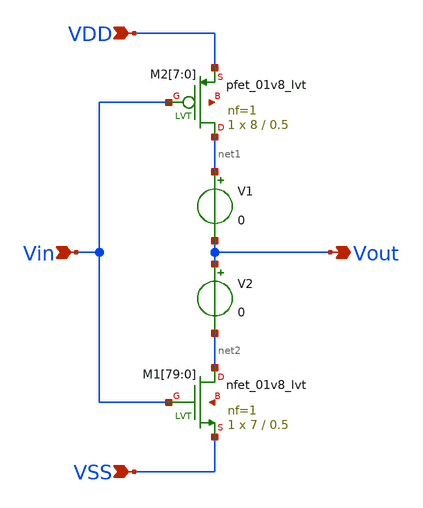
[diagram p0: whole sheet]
** sch_path: design/THESIS_EXP_RO_INVERTER_SKY130A/INV_LVT_v2.sch
**.subckt INV_LVT_v2 VDD VSS Vin Vout
*.ipin VDD
*.ipin VSS
*.ipin Vin
*.opin Vout
XM1[79] net2 Vin VSS net3[79] sky130_fd_pr__nfet_01v8_lvt L=0.5 W=7 nf=1 ad='int((nf+1)/2) * W/nf * 0.29'
+ as='int((nf+2)/2) * W/nf * 0.29' pd='2*int((nf+1)/2) * (W/nf + 0.29)' ps='2*int((nf+2)/2) * (W/nf + 0.29)'
+ nrd='0.29 / W' nrs='0.29 / W' sa=0 sb=0 sd=0 mult=1 m=1
XM1[78] net2 Vin VSS net3[78] sky130_fd_pr__nfet_01v8_lvt L=0.5 W=7 nf=1 ad='int((nf+1)/2) * W/nf * 0.29'
+ as='int((nf+2)/2) * W/nf * 0.29' pd='2*int((nf+1)/2) * (W/nf + 0.29)' ps='2*int((nf+2)/2) * (W/nf + 0.29)'
+ nrd='0.29 / W' nrs='0.29 / W' sa=0 sb=0 sd=0 mult=1 m=1
XM1[77] net2 Vin VSS net3[77] sky130_fd_pr__nfet_01v8_lvt L=0.5 W=7 nf=1 ad='int((nf+1)/2) * W/nf * 0.29'
+ as='int((nf+2)/2) * W/nf * 0.29' pd='2*int((nf+1)/2) * (W/nf + 0.29)' ps='2*int((nf+2)/2) * (W/nf + 0.29)'
+ nrd='0.29 / W' nrs='0.29 / W' sa=0 sb=0 sd=0 mult=1 m=1
XM1[76] net2 Vin VSS net3[76] sky130_fd_pr__nfet_01v8_lvt L=0.5 W=7 nf=1 ad='int((nf+1)/2) * W/nf * 0.29'
+ as='int((nf+2)/2) * W/nf * 0.29' pd='2*int((nf+1)/2) * (W/nf + 0.29)' ps='2*int((nf+2)/2) * (W/nf + 0.29)'
+ nrd='0.29 / W' nrs='0.29 / W' sa=0 sb=0 sd=0 mult=1 m=1
XM1[75] net2 Vin VSS net3[75] sky130_fd_pr__nfet_01v8_lvt L=0.5 W=7 nf=1 ad='int((nf+1)/2) * W/nf * 0.29'
+ as='int((nf+2)/2) * W/nf * 0.29' pd='2*int((nf+1)/2) * (W/nf + 0.29)' ps='2*int((nf+2)/2) * (W/nf + 0.29)'
+ nrd='0.29 / W' nrs='0.29 / W' sa=0 sb=0 sd=0 mult=1 m=1
XM1[74] net2 Vin VSS net3[74] sky130_fd_pr__nfet_01v8_lvt L=0.5 W=7 nf=1 ad='int((nf+1)/2) * W/nf * 0.29'
+ as='int((nf+2)/2) * W/nf * 0.29' pd='2*int((nf+1)/2) * (W/nf + 0.29)' ps='2*int((nf+2)/2) * (W/nf + 0.29)'
+ nrd='0.29 / W' nrs='0.29 / W' sa=0 sb=0 sd=0 mult=1 m=1
XM1[73] net2 Vin VSS net3[73] sky130_fd_pr__nfet_01v8_lvt L=0.5 W=7 nf=1 ad='int((nf+1)/2) * W/nf * 0.29'
+ as='int((nf+2)/2) * W/nf * 0.29' pd='2*int((nf+1)/2) * (W/nf + 0.29)' ps='2*int((nf+2)/2) * (W/nf + 0.29)'
+ nrd='0.29 / W' nrs='0.29 / W' sa=0 sb=0 sd=0 mult=1 m=1
XM1[72] net2 Vin VSS net3[72] sky130_fd_pr__nfet_01v8_lvt L=0.5 W=7 nf=1 ad='int((nf+1)/2) * W/nf * 0.29'
+ as='int((nf+2)/2) * W/nf * 0.29' pd='2*int((nf+1)/2) * (W/nf + 0.29)' ps='2*int((nf+2)/2) * (W/nf + 0.29)'
+ nrd='0.29 / W' nrs='0.29 / W' sa=0 sb=0 sd=0 mult=1 m=1
XM1[71] net2 Vin VSS net3[71] sky130_fd_pr__nfet_01v8_lvt L=0.5 W=7 nf=1 ad='int((nf+1)/2) * W/nf * 0.29'
+ as='int((nf+2)/2) * W/nf * 0.29' pd='2*int((nf+1)/2) * (W/nf + 0.29)' ps='2*int((nf+2)/2) * (W/nf + 0.29)'
+ nrd='0.29 / W' nrs='0.29 / W' sa=0 sb=0 sd=0 mult=1 m=1
XM1[70] net2 Vin VSS net3[70] sky130_fd_pr__nfet_01v8_lvt L=0.5 W=7 nf=1 ad='int((nf+1)/2) * W/nf * 0.29'
+ as='int((nf+2)/2) * W/nf * 0.29' pd='2*int((nf+1)/2) * (W/nf + 0.29)' ps='2*int((nf+2)/2) * (W/nf + 0.29)'
+ nrd='0.29 / W' nrs='0.29 / W' sa=0 sb=0 sd=0 mult=1 m=1
XM1[69] net2 Vin VSS net3[69] sky130_fd_pr__nfet_01v8_lvt L=0.5 W=7 nf=1 ad='int((nf+1)/2) * W/nf * 0.29'
+ as='int((nf+2)/2) * W/nf * 0.29' pd='2*int((nf+1)/2) * (W/nf + 0.29)' ps='2*int((nf+2)/2) * (W/nf + 0.29)'
+ nrd='0.29 / W' nrs='0.29 / W' sa=0 sb=0 sd=0 mult=1 m=1
XM1[68] net2 Vin VSS net3[68] sky130_fd_pr__nfet_01v8_lvt L=0.5 W=7 nf=1 ad='int((nf+1)/2) * W/nf * 0.29'
+ as='int((nf+2)/2) * W/nf * 0.29' pd='2*int((nf+1)/2) * (W/nf + 0.29)' ps='2*int((nf+2)/2) * (W/nf + 0.29)'
+ nrd='0.29 / W' nrs='0.29 / W' sa=0 sb=0 sd=0 mult=1 m=1
XM1[67] net2 Vin VSS net3[67] sky130_fd_pr__nfet_01v8_lvt L=0.5 W=7 nf=1 ad='int((nf+1)/2) * W/nf * 0.29'
+ as='int((nf+2)/2) * W/nf * 0.29' pd='2*int((nf+1)/2) * (W/nf + 0.29)' ps='2*int((nf+2)/2) * (W/nf + 0.29)'
+ nrd='0.29 / W' nrs='0.29 / W' sa=0 sb=0 sd=0 mult=1 m=1
XM1[66] net2 Vin VSS net3[66] sky130_fd_pr__nfet_01v8_lvt L=0.5 W=7 nf=1 ad='int((nf+1)/2) * W/nf * 0.29'
+ as='int((nf+2)/2) * W/nf * 0.29' pd='2*int((nf+1)/2) * (W/nf + 0.29)' ps='2*int((nf+2)/2) * (W/nf + 0.29)'
+ nrd='0.29 / W' nrs='0.29 / W' sa=0 sb=0 sd=0 mult=1 m=1
XM1[65] net2 Vin VSS net3[65] sky130_fd_pr__nfet_01v8_lvt L=0.5 W=7 nf=1 ad='int((nf+1)/2) * W/nf * 0.29'
+ as='int((nf+2)/2) * W/nf * 0.29' pd='2*int((nf+1)/2) * (W/nf + 0.29)' ps='2*int((nf+2)/2) * (W/nf + 0.29)'
+ nrd='0.29 / W' nrs='0.29 / W' sa=0 sb=0 sd=0 mult=1 m=1
XM1[64] net2 Vin VSS net3[64] sky130_fd_pr__nfet_01v8_lvt L=0.5 W=7 nf=1 ad='int((nf+1)/2) * W/nf * 0.29'
+ as='int((nf+2)/2) * W/nf * 0.29' pd='2*int((nf+1)/2) * (W/nf + 0.29)' ps='2*int((nf+2)/2) * (W/nf + 0.29)'
+ nrd='0.29 / W' nrs='0.29 / W' sa=0 sb=0 sd=0 mult=1 m=1
XM1[63] net2 Vin VSS net3[63] sky130_fd_pr__nfet_01v8_lvt L=0.5 W=7 nf=1 ad='int((nf+1)/2) * W/nf * 0.29'
+ as='int((nf+2)/2) * W/nf * 0.29' pd='2*int((nf+1)/2) * (W/nf + 0.29)' ps='2*int((nf+2)/2) * (W/nf + 0.29)'
+ nrd='0.29 / W' nrs='0.29 / W' sa=0 sb=0 sd=0 mult=1 m=1
XM1[62] net2 Vin VSS net3[62] sky130_fd_pr__nfet_01v8_lvt L=0.5 W=7 nf=1 ad='int((nf+1)/2) * W/nf * 0.29'
+ as='int((nf+2)/2) * W/nf * 0.29' pd='2*int((nf+1)/2) * (W/nf + 0.29)' ps='2*int((nf+2)/2) * (W/nf + 0.29)'
+ nrd='0.29 / W' nrs='0.29 / W' sa=0 sb=0 sd=0 mult=1 m=1
XM1[61] net2 Vin VSS net3[61] sky130_fd_pr__nfet_01v8_lvt L=0.5 W=7 nf=1 ad='int((nf+1)/2) * W/nf * 0.29'
+ as='int((nf+2)/2) * W/nf * 0.29' pd='2*int((nf+1)/2) * (W/nf + 0.29)' ps='2*int((nf+2)/2) * (W/nf + 0.29)'
+ nrd='0.29 / W' nrs='0.29 / W' sa=0 sb=0 sd=0 mult=1 m=1
XM1[60] net2 Vin VSS net3[60] sky130_fd_pr__nfet_01v8_lvt L=0.5 W=7 nf=1 ad='int((nf+1)/2) * W/nf * 0.29'
+ as='int((nf+2)/2) * W/nf * 0.29' pd='2*int((nf+1)/2) * (W/nf + 0.29)' ps='2*int((nf+2)/2) * (W/nf + 0.29)'
+ nrd='0.29 / W' nrs='0.29 / W' sa=0 sb=0 sd=0 mult=1 m=1
XM1[59] net2 Vin VSS net3[59] sky130_fd_pr__nfet_01v8_lvt L=0.5 W=7 nf=1 ad='int((nf+1)/2) * W/nf * 0.29'
+ as='int((nf+2)/2) * W/nf * 0.29' pd='2*int((nf+1)/2) * (W/nf + 0.29)' ps='2*int((nf+2)/2) * (W/nf + 0.29)'
+ nrd='0.29 / W' nrs='0.29 / W' sa=0 sb=0 sd=0 mult=1 m=1
XM1[58] net2 Vin VSS net3[58] sky130_fd_pr__nfet_01v8_lvt L=0.5 W=7 nf=1 ad='int((nf+1)/2) * W/nf * 0.29'
+ as='int((nf+2)/2) * W/nf * 0.29' pd='2*int((nf+1)/2) * (W/nf + 0.29)' ps='2*int((nf+2)/2) * (W/nf + 0.29)'
+ nrd='0.29 / W' nrs='0.29 / W' sa=0 sb=0 sd=0 mult=1 m=1
XM1[57] net2 Vin VSS net3[57] sky130_fd_pr__nfet_01v8_lvt L=0.5 W=7 nf=1 ad='int((nf+1)/2) * W/nf * 0.29'
+ as='int((nf+2)/2) * W/nf * 0.29' pd='2*int((nf+1)/2) * (W/nf + 0.29)' ps='2*int((nf+2)/2) * (W/nf + 0.29)'
+ nrd='0.29 / W' nrs='0.29 / W' sa=0 sb=0 sd=0 mult=1 m=1
XM1[56] net2 Vin VSS net3[56] sky130_fd_pr__nfet_01v8_lvt L=0.5 W=7 nf=1 ad='int((nf+1)/2) * W/nf * 0.29'
+ as='int((nf+2)/2) * W/nf * 0.29' pd='2*int((nf+1)/2) * (W/nf + 0.29)' ps='2*int((nf+2)/2) * (W/nf + 0.29)'
+ nrd='0.29 / W' nrs='0.29 / W' sa=0 sb=0 sd=0 mult=1 m=1
XM1[55] net2 Vin VSS net3[55] sky130_fd_pr__nfet_01v8_lvt L=0.5 W=7 nf=1 ad='int((nf+1)/2) * W/nf * 0.29'
+ as='int((nf+2)/2) * W/nf * 0.29' pd='2*int((nf+1)/2) * (W/nf + 0.29)' ps='2*int((nf+2)/2) * (W/nf + 0.29)'
+ nrd='0.29 / W' nrs='0.29 / W' sa=0 sb=0 sd=0 mult=1 m=1
XM1[54] net2 Vin VSS net3[54] sky130_fd_pr__nfet_01v8_lvt L=0.5 W=7 nf=1 ad='int((nf+1)/2) * W/nf * 0.29'
+ as='int((nf+2)/2) * W/nf * 0.29' pd='2*int((nf+1)/2) * (W/nf + 0.29)' ps='2*int((nf+2)/2) * (W/nf + 0.29)'
+ nrd='0.29 / W' nrs='0.29 / W' sa=0 sb=0 sd=0 mult=1 m=1
XM1[53] net2 Vin VSS net3[53] sky130_fd_pr__nfet_01v8_lvt L=0.5 W=7 nf=1 ad='int((nf+1)/2) * W/nf * 0.29'
+ as='int((nf+2)/2) * W/nf * 0.29' pd='2*int((nf+1)/2) * (W/nf + 0.29)' ps='2*int((nf+2)/2) * (W/nf + 0.29)'
+ nrd='0.29 / W' nrs='0.29 / W' sa=0 sb=0 sd=0 mult=1 m=1
XM1[52] net2 Vin VSS net3[52] sky130_fd_pr__nfet_01v8_lvt L=0.5 W=7 nf=1 ad='int((nf+1)/2) * W/nf * 0.29'
+ as='int((nf+2)/2) * W/nf * 0.29' pd='2*int((nf+1)/2) * (W/nf + 0.29)' ps='2*int((nf+2)/2) * (W/nf + 0.29)'
+ nrd='0.29 / W' nrs='0.29 / W' sa=0 sb=0 sd=0 mult=1 m=1
XM1[51] net2 Vin VSS net3[51] sky130_fd_pr__nfet_01v8_lvt L=0.5 W=7 nf=1 ad='int((nf+1)/2) * W/nf * 0.29'
+ as='int((nf+2)/2) * W/nf * 0.29' pd='2*int((nf+1)/2) * (W/nf + 0.29)' ps='2*int((nf+2)/2) * (W/nf + 0.29)'
+ nrd='0.29 / W' nrs='0.29 / W' sa=0 sb=0 sd=0 mult=1 m=1
XM1[50] net2 Vin VSS net3[50] sky130_fd_pr__nfet_01v8_lvt L=0.5 W=7 nf=1 ad='int((nf+1)/2) * W/nf * 0.29'
+ as='int((nf+2)/2) * W/nf * 0.29' pd='2*int((nf+1)/2) * (W/nf + 0.29)' ps='2*int((nf+2)/2) * (W/nf + 0.29)'
+ nrd='0.29 / W' nrs='0.29 / W' sa=0 sb=0 sd=0 mult=1 m=1
XM1[49] net2 Vin VSS net3[49] sky130_fd_pr__nfet_01v8_lvt L=0.5 W=7 nf=1 ad='int((nf+1)/2) * W/nf * 0.29'
+ as='int((nf+2)/2) * W/nf * 0.29' pd='2*int((nf+1)/2) * (W/nf + 0.29)' ps='2*int((nf+2)/2) * (W/nf + 0.29)'
+ nrd='0.29 / W' nrs='0.29 / W' sa=0 sb=0 sd=0 mult=1 m=1
XM1[48] net2 Vin VSS net3[48] sky130_fd_pr__nfet_01v8_lvt L=0.5 W=7 nf=1 ad='int((nf+1)/2) * W/nf * 0.29'
+ as='int((nf+2)/2) * W/nf * 0.29' pd='2*int((nf+1)/2) * (W/nf + 0.29)' ps='2*int((nf+2)/2) * (W/nf + 0.29)'
+ nrd='0.29 / W' nrs='0.29 / W' sa=0 sb=0 sd=0 mult=1 m=1
XM1[47] net2 Vin VSS net3[47] sky130_fd_pr__nfet_01v8_lvt L=0.5 W=7 nf=1 ad='int((nf+1)/2) * W/nf * 0.29'
+ as='int((nf+2)/2) * W/nf * 0.29' pd='2*int((nf+1)/2) * (W/nf + 0.29)' ps='2*int((nf+2)/2) * (W/nf + 0.29)'
+ nrd='0.29 / W' nrs='0.29 / W' sa=0 sb=0 sd=0 mult=1 m=1
XM1[46] net2 Vin VSS net3[46] sky130_fd_pr__nfet_01v8_lvt L=0.5 W=7 nf=1 ad='int((nf+1)/2) * W/nf * 0.29'
+ as='int((nf+2)/2) * W/nf * 0.29' pd='2*int((nf+1)/2) * (W/nf + 0.29)' ps='2*int((nf+2)/2) * (W/nf + 0.29)'
+ nrd='0.29 / W' nrs='0.29 / W' sa=0 sb=0 sd=0 mult=1 m=1
XM1[45] net2 Vin VSS net3[45] sky130_fd_pr__nfet_01v8_lvt L=0.5 W=7 nf=1 ad='int((nf+1)/2) * W/nf * 0.29'
+ as='int((nf+2)/2) * W/nf * 0.29' pd='2*int((nf+1)/2) * (W/nf + 0.29)' ps='2*int((nf+2)/2) * (W/nf + 0.29)'
+ nrd='0.29 / W' nrs='0.29 / W' sa=0 sb=0 sd=0 mult=1 m=1
XM1[44] net2 Vin VSS net3[44] sky130_fd_pr__nfet_01v8_lvt L=0.5 W=7 nf=1 ad='int((nf+1)/2) * W/nf * 0.29'
+ as='int((nf+2)/2) * W/nf * 0.29' pd='2*int((nf+1)/2) * (W/nf + 0.29)' ps='2*int((nf+2)/2) * (W/nf + 0.29)'
+ nrd='0.29 / W' nrs='0.29 / W' sa=0 sb=0 sd=0 mult=1 m=1
XM1[43] net2 Vin VSS net3[43] sky130_fd_pr__nfet_01v8_lvt L=0.5 W=7 nf=1 ad='int((nf+1)/2) * W/nf * 0.29'
+ as='int((nf+2)/2) * W/nf * 0.29' pd='2*int((nf+1)/2) * (W/nf + 0.29)' ps='2*int((nf+2)/2) * (W/nf + 0.29)'
+ nrd='0.29 / W' nrs='0.29 / W' sa=0 sb=0 sd=0 mult=1 m=1
XM1[42] net2 Vin VSS net3[42] sky130_fd_pr__nfet_01v8_lvt L=0.5 W=7 nf=1 ad='int((nf+1)/2) * W/nf * 0.29'
+ as='int((nf+2)/2) * W/nf * 0.29' pd='2*int((nf+1)/2) * (W/nf + 0.29)' ps='2*int((nf+2)/2) * (W/nf + 0.29)'
+ nrd='0.29 / W' nrs='0.29 / W' sa=0 sb=0 sd=0 mult=1 m=1
XM1[41] net2 Vin VSS net3[41] sky130_fd_pr__nfet_01v8_lvt L=0.5 W=7 nf=1 ad='int((nf+1)/2) * W/nf * 0.29'
+ as='int((nf+2)/2) * W/nf * 0.29' pd='2*int((nf+1)/2) * (W/nf + 0.29)' ps='2*int((nf+2)/2) * (W/nf + 0.29)'
+ nrd='0.29 / W' nrs='0.29 / W' sa=0 sb=0 sd=0 mult=1 m=1
XM1[40] net2 Vin VSS net3[40] sky130_fd_pr__nfet_01v8_lvt L=0.5 W=7 nf=1 ad='int((nf+1)/2) * W/nf * 0.29'
+ as='int((nf+2)/2) * W/nf * 0.29' pd='2*int((nf+1)/2) * (W/nf + 0.29)' ps='2*int((nf+2)/2) * (W/nf + 0.29)'
+ nrd='0.29 / W' nrs='0.29 / W' sa=0 sb=0 sd=0 mult=1 m=1
XM1[39] net2 Vin VSS net3[39] sky130_fd_pr__nfet_01v8_lvt L=0.5 W=7 nf=1 ad='int((nf+1)/2) * W/nf * 0.29'
+ as='int((nf+2)/2) * W/nf * 0.29' pd='2*int((nf+1)/2) * (W/nf + 0.29)' ps='2*int((nf+2)/2) * (W/nf + 0.29)'
+ nrd='0.29 / W' nrs='0.29 / W' sa=0 sb=0 sd=0 mult=1 m=1
XM1[38] net2 Vin VSS net3[38] sky130_fd_pr__nfet_01v8_lvt L=0.5 W=7 nf=1 ad='int((nf+1)/2) * W/nf * 0.29'
+ as='int((nf+2)/2) * W/nf * 0.29' pd='2*int((nf+1)/2) * (W/nf + 0.29)' ps='2*int((nf+2)/2) * (W/nf + 0.29)'
+ nrd='0.29 / W' nrs='0.29 / W' sa=0 sb=0 sd=0 mult=1 m=1
XM1[37] net2 Vin VSS net3[37] sky130_fd_pr__nfet_01v8_lvt L=0.5 W=7 nf=1 ad='int((nf+1)/2) * W/nf * 0.29'
+ as='int((nf+2)/2) * W/nf * 0.29' pd='2*int((nf+1)/2) * (W/nf + 0.29)' ps='2*int((nf+2)/2) * (W/nf + 0.29)'
+ nrd='0.29 / W' nrs='0.29 / W' sa=0 sb=0 sd=0 mult=1 m=1
XM1[36] net2 Vin VSS net3[36] sky130_fd_pr__nfet_01v8_lvt L=0.5 W=7 nf=1 ad='int((nf+1)/2) * W/nf * 0.29'
+ as='int((nf+2)/2) * W/nf * 0.29' pd='2*int((nf+1)/2) * (W/nf + 0.29)' ps='2*int((nf+2)/2) * (W/nf + 0.29)'
+ nrd='0.29 / W' nrs='0.29 / W' sa=0 sb=0 sd=0 mult=1 m=1
XM1[35] net2 Vin VSS net3[35] sky130_fd_pr__nfet_01v8_lvt L=0.5 W=7 nf=1 ad='int((nf+1)/2) * W/nf * 0.29'
+ as='int((nf+2)/2) * W/nf * 0.29' pd='2*int((nf+1)/2) * (W/nf + 0.29)' ps='2*int((nf+2)/2) * (W/nf + 0.29)'
+ nrd='0.29 / W' nrs='0.29 / W' sa=0 sb=0 sd=0 mult=1 m=1
XM1[34] net2 Vin VSS net3[34] sky130_fd_pr__nfet_01v8_lvt L=0.5 W=7 nf=1 ad='int((nf+1)/2) * W/nf * 0.29'
+ as='int((nf+2)/2) * W/nf * 0.29' pd='2*int((nf+1)/2) * (W/nf + 0.29)' ps='2*int((nf+2)/2) * (W/nf + 0.29)'
+ nrd='0.29 / W' nrs='0.29 / W' sa=0 sb=0 sd=0 mult=1 m=1
XM1[33] net2 Vin VSS net3[33] sky130_fd_pr__nfet_01v8_lvt L=0.5 W=7 nf=1 ad='int((nf+1)/2) * W/nf * 0.29'
+ as='int((nf+2)/2) * W/nf * 0.29' pd='2*int((nf+1)/2) * (W/nf + 0.29)' ps='2*int((nf+2)/2) * (W/nf + 0.29)'
+ nrd='0.29 / W' nrs='0.29 / W' sa=0 sb=0 sd=0 mult=1 m=1
XM1[32] net2 Vin VSS net3[32] sky130_fd_pr__nfet_01v8_lvt L=0.5 W=7 nf=1 ad='int((nf+1)/2) * W/nf * 0.29'
+ as='int((nf+2)/2) * W/nf * 0.29' pd='2*int((nf+1)/2) * (W/nf + 0.29)' ps='2*int((nf+2)/2) * (W/nf + 0.29)'
+ nrd='0.29 / W' nrs='0.29 / W' sa=0 sb=0 sd=0 mult=1 m=1
XM1[31] net2 Vin VSS net3[31] sky130_fd_pr__nfet_01v8_lvt L=0.5 W=7 nf=1 ad='int((nf+1)/2) * W/nf * 0.29'
+ as='int((nf+2)/2) * W/nf * 0.29' pd='2*int((nf+1)/2) * (W/nf + 0.29)' ps='2*int((nf+2)/2) * (W/nf + 0.29)'
+ nrd='0.29 / W' nrs='0.29 / W' sa=0 sb=0 sd=0 mult=1 m=1
XM1[30] net2 Vin VSS net3[30] sky130_fd_pr__nfet_01v8_lvt L=0.5 W=7 nf=1 ad='int((nf+1)/2) * W/nf * 0.29'
+ as='int((nf+2)/2) * W/nf * 0.29' pd='2*int((nf+1)/2) * (W/nf + 0.29)' ps='2*int((nf+2)/2) * (W/nf + 0.29)'
+ nrd='0.29 / W' nrs='0.29 / W' sa=0 sb=0 sd=0 mult=1 m=1
XM1[29] net2 Vin VSS net3[29] sky130_fd_pr__nfet_01v8_lvt L=0.5 W=7 nf=1 ad='int((nf+1)/2) * W/nf * 0.29'
+ as='int((nf+2)/2) * W/nf * 0.29' pd='2*int((nf+1)/2) * (W/nf + 0.29)' ps='2*int((nf+2)/2) * (W/nf + 0.29)'
+ nrd='0.29 / W' nrs='0.29 / W' sa=0 sb=0 sd=0 mult=1 m=1
XM1[28] net2 Vin VSS net3[28] sky130_fd_pr__nfet_01v8_lvt L=0.5 W=7 nf=1 ad='int((nf+1)/2) * W/nf * 0.29'
+ as='int((nf+2)/2) * W/nf * 0.29' pd='2*int((nf+1)/2) * (W/nf + 0.29)' ps='2*int((nf+2)/2) * (W/nf + 0.29)'
+ nrd='0.29 / W' nrs='0.29 / W' sa=0 sb=0 sd=0 mult=1 m=1
XM1[27] net2 Vin VSS net3[27] sky130_fd_pr__nfet_01v8_lvt L=0.5 W=7 nf=1 ad='int((nf+1)/2) * W/nf * 0.29'
+ as='int((nf+2)/2) * W/nf * 0.29' pd='2*int((nf+1)/2) * (W/nf + 0.29)' ps='2*int((nf+2)/2) * (W/nf + 0.29)'
+ nrd='0.29 / W' nrs='0.29 / W' sa=0 sb=0 sd=0 mult=1 m=1
XM1[26] net2 Vin VSS net3[26] sky130_fd_pr__nfet_01v8_lvt L=0.5 W=7 nf=1 ad='int((nf+1)/2) * W/nf * 0.29'
+ as='int((nf+2)/2) * W/nf * 0.29' pd='2*int((nf+1)/2) * (W/nf + 0.29)' ps='2*int((nf+2)/2) * (W/nf + 0.29)'
+ nrd='0.29 / W' nrs='0.29 / W' sa=0 sb=0 sd=0 mult=1 m=1
XM1[25] net2 Vin VSS net3[25] sky130_fd_pr__nfet_01v8_lvt L=0.5 W=7 nf=1 ad='int((nf+1)/2) * W/nf * 0.29'
+ as='int((nf+2)/2) * W/nf * 0.29' pd='2*int((nf+1)/2) * (W/nf + 0.29)' ps='2*int((nf+2)/2) * (W/nf + 0.29)'
+ nrd='0.29 / W' nrs='0.29 / W' sa=0 sb=0 sd=0 mult=1 m=1
XM1[24] net2 Vin VSS net3[24] sky130_fd_pr__nfet_01v8_lvt L=0.5 W=7 nf=1 ad='int((nf+1)/2) * W/nf * 0.29'
+ as='int((nf+2)/2) * W/nf * 0.29' pd='2*int((nf+1)/2) * (W/nf + 0.29)' ps='2*int((nf+2)/2) * (W/nf + 0.29)'
+ nrd='0.29 / W' nrs='0.29 / W' sa=0 sb=0 sd=0 mult=1 m=1
XM1[23] net2 Vin VSS net3[23] sky130_fd_pr__nfet_01v8_lvt L=0.5 W=7 nf=1 ad='int((nf+1)/2) * W/nf * 0.29'
+ as='int((nf+2)/2) * W/nf * 0.29' pd='2*int((nf+1)/2) * (W/nf + 0.29)' ps='2*int((nf+2)/2) * (W/nf + 0.29)'
+ nrd='0.29 / W' nrs='0.29 / W' sa=0 sb=0 sd=0 mult=1 m=1
XM1[22] net2 Vin VSS net3[22] sky130_fd_pr__nfet_01v8_lvt L=0.5 W=7 nf=1 ad='int((nf+1)/2) * W/nf * 0.29'
+ as='int((nf+2)/2) * W/nf * 0.29' pd='2*int((nf+1)/2) * (W/nf + 0.29)' ps='2*int((nf+2)/2) * (W/nf + 0.29)'
+ nrd='0.29 / W' nrs='0.29 / W' sa=0 sb=0 sd=0 mult=1 m=1
XM1[21] net2 Vin VSS net3[21] sky130_fd_pr__nfet_01v8_lvt L=0.5 W=7 nf=1 ad='int((nf+1)/2) * W/nf * 0.29'
+ as='int((nf+2)/2) * W/nf * 0.29' pd='2*int((nf+1)/2) * (W/nf + 0.29)' ps='2*int((nf+2)/2) * (W/nf + 0.29)'
+ nrd='0.29 / W' nrs='0.29 / W' sa=0 sb=0 sd=0 mult=1 m=1
XM1[20] net2 Vin VSS net3[20] sky130_fd_pr__nfet_01v8_lvt L=0.5 W=7 nf=1 ad='int((nf+1)/2) * W/nf * 0.29'
+ as='int((nf+2)/2) * W/nf * 0.29' pd='2*int((nf+1)/2) * (W/nf + 0.29)' ps='2*int((nf+2)/2) * (W/nf + 0.29)'
+ nrd='0.29 / W' nrs='0.29 / W' sa=0 sb=0 sd=0 mult=1 m=1
XM1[19] net2 Vin VSS net3[19] sky130_fd_pr__nfet_01v8_lvt L=0.5 W=7 nf=1 ad='int((nf+1)/2) * W/nf * 0.29'
+ as='int((nf+2)/2) * W/nf * 0.29' pd='2*int((nf+1)/2) * (W/nf + 0.29)' ps='2*int((nf+2)/2) * (W/nf + 0.29)'
+ nrd='0.29 / W' nrs='0.29 / W' sa=0 sb=0 sd=0 mult=1 m=1
XM1[18] net2 Vin VSS net3[18] sky130_fd_pr__nfet_01v8_lvt L=0.5 W=7 nf=1 ad='int((nf+1)/2) * W/nf * 0.29'
+ as='int((nf+2)/2) * W/nf * 0.29' pd='2*int((nf+1)/2) * (W/nf + 0.29)' ps='2*int((nf+2)/2) * (W/nf + 0.29)'
+ nrd='0.29 / W' nrs='0.29 / W' sa=0 sb=0 sd=0 mult=1 m=1
XM1[17] net2 Vin VSS net3[17] sky130_fd_pr__nfet_01v8_lvt L=0.5 W=7 nf=1 ad='int((nf+1)/2) * W/nf * 0.29'
+ as='int((nf+2)/2) * W/nf * 0.29' pd='2*int((nf+1)/2) * (W/nf + 0.29)' ps='2*int((nf+2)/2) * (W/nf + 0.29)'
+ nrd='0.29 / W' nrs='0.29 / W' sa=0 sb=0 sd=0 mult=1 m=1
XM1[16] net2 Vin VSS net3[16] sky130_fd_pr__nfet_01v8_lvt L=0.5 W=7 nf=1 ad='int((nf+1)/2) * W/nf * 0.29'
+ as='int((nf+2)/2) * W/nf * 0.29' pd='2*int((nf+1)/2) * (W/nf + 0.29)' ps='2*int((nf+2)/2) * (W/nf + 0.29)'
+ nrd='0.29 / W' nrs='0.29 / W' sa=0 sb=0 sd=0 mult=1 m=1
XM1[15] net2 Vin VSS net3[15] sky130_fd_pr__nfet_01v8_lvt L=0.5 W=7 nf=1 ad='int((nf+1)/2) * W/nf * 0.29'
+ as='int((nf+2)/2) * W/nf * 0.29' pd='2*int((nf+1)/2) * (W/nf + 0.29)' ps='2*int((nf+2)/2) * (W/nf + 0.29)'
+ nrd='0.29 / W' nrs='0.29 / W' sa=0 sb=0 sd=0 mult=1 m=1
XM1[14] net2 Vin VSS net3[14] sky130_fd_pr__nfet_01v8_lvt L=0.5 W=7 nf=1 ad='int((nf+1)/2) * W/nf * 0.29'
+ as='int((nf+2)/2) * W/nf * 0.29' pd='2*int((nf+1)/2) * (W/nf + 0.29)' ps='2*int((nf+2)/2) * (W/nf + 0.29)'
+ nrd='0.29 / W' nrs='0.29 / W' sa=0 sb=0 sd=0 mult=1 m=1
XM1[13] net2 Vin VSS net3[13] sky130_fd_pr__nfet_01v8_lvt L=0.5 W=7 nf=1 ad='int((nf+1)/2) * W/nf * 0.29'
+ as='int((nf+2)/2) * W/nf * 0.29' pd='2*int((nf+1)/2) * (W/nf + 0.29)' ps='2*int((nf+2)/2) * (W/nf + 0.29)'
+ nrd='0.29 / W' nrs='0.29 / W' sa=0 sb=0 sd=0 mult=1 m=1
XM1[12] net2 Vin VSS net3[12] sky130_fd_pr__nfet_01v8_lvt L=0.5 W=7 nf=1 ad='int((nf+1)/2) * W/nf * 0.29'
+ as='int((nf+2)/2) * W/nf * 0.29' pd='2*int((nf+1)/2) * (W/nf + 0.29)' ps='2*int((nf+2)/2) * (W/nf + 0.29)'
+ nrd='0.29 / W' nrs='0.29 / W' sa=0 sb=0 sd=0 mult=1 m=1
XM1[11] net2 Vin VSS net3[11] sky130_fd_pr__nfet_01v8_lvt L=0.5 W=7 nf=1 ad='int((nf+1)/2) * W/nf * 0.29'
+ as='int((nf+2)/2) * W/nf * 0.29' pd='2*int((nf+1)/2) * (W/nf + 0.29)' ps='2*int((nf+2)/2) * (W/nf + 0.29)'
+ nrd='0.29 / W' nrs='0.29 / W' sa=0 sb=0 sd=0 mult=1 m=1
XM1[10] net2 Vin VSS net3[10] sky130_fd_pr__nfet_01v8_lvt L=0.5 W=7 nf=1 ad='int((nf+1)/2) * W/nf * 0.29'
+ as='int((nf+2)/2) * W/nf * 0.29' pd='2*int((nf+1)/2) * (W/nf + 0.29)' ps='2*int((nf+2)/2) * (W/nf + 0.29)'
+ nrd='0.29 / W' nrs='0.29 / W' sa=0 sb=0 sd=0 mult=1 m=1
XM1[9] net2 Vin VSS net3[9] sky130_fd_pr__nfet_01v8_lvt L=0.5 W=7 nf=1 ad='int((nf+1)/2) * W/nf * 0.29'
+ as='int((nf+2)/2) * W/nf * 0.29' pd='2*int((nf+1)/2) * (W/nf + 0.29)' ps='2*int((nf+2)/2) * (W/nf + 0.29)'
+ nrd='0.29 / W' nrs='0.29 / W' sa=0 sb=0 sd=0 mult=1 m=1
XM1[8] net2 Vin VSS net3[8] sky130_fd_pr__nfet_01v8_lvt L=0.5 W=7 nf=1 ad='int((nf+1)/2) * W/nf * 0.29'
+ as='int((nf+2)/2) * W/nf * 0.29' pd='2*int((nf+1)/2) * (W/nf + 0.29)' ps='2*int((nf+2)/2) * (W/nf + 0.29)'
+ nrd='0.29 / W' nrs='0.29 / W' sa=0 sb=0 sd=0 mult=1 m=1
XM1[7] net2 Vin VSS net3[7] sky130_fd_pr__nfet_01v8_lvt L=0.5 W=7 nf=1 ad='int((nf+1)/2) * W/nf * 0.29'
+ as='int((nf+2)/2) * W/nf * 0.29' pd='2*int((nf+1)/2) * (W/nf + 0.29)' ps='2*int((nf+2)/2) * (W/nf + 0.29)'
+ nrd='0.29 / W' nrs='0.29 / W' sa=0 sb=0 sd=0 mult=1 m=1
XM1[6] net2 Vin VSS net3[6] sky130_fd_pr__nfet_01v8_lvt L=0.5 W=7 nf=1 ad='int((nf+1)/2) * W/nf * 0.29'
+ as='int((nf+2)/2) * W/nf * 0.29' pd='2*int((nf+1)/2) * (W/nf + 0.29)' ps='2*int((nf+2)/2) * (W/nf + 0.29)'
+ nrd='0.29 / W' nrs='0.29 / W' sa=0 sb=0 sd=0 mult=1 m=1
XM1[5] net2 Vin VSS net3[5] sky130_fd_pr__nfet_01v8_lvt L=0.5 W=7 nf=1 ad='int((nf+1)/2) * W/nf * 0.29'
+ as='int((nf+2)/2) * W/nf * 0.29' pd='2*int((nf+1)/2) * (W/nf + 0.29)' ps='2*int((nf+2)/2) * (W/nf + 0.29)'
+ nrd='0.29 / W' nrs='0.29 / W' sa=0 sb=0 sd=0 mult=1 m=1
XM1[4] net2 Vin VSS net3[4] sky130_fd_pr__nfet_01v8_lvt L=0.5 W=7 nf=1 ad='int((nf+1)/2) * W/nf * 0.29'
+ as='int((nf+2)/2) * W/nf * 0.29' pd='2*int((nf+1)/2) * (W/nf + 0.29)' ps='2*int((nf+2)/2) * (W/nf + 0.29)'
+ nrd='0.29 / W' nrs='0.29 / W' sa=0 sb=0 sd=0 mult=1 m=1
XM1[3] net2 Vin VSS net3[3] sky130_fd_pr__nfet_01v8_lvt L=0.5 W=7 nf=1 ad='int((nf+1)/2) * W/nf * 0.29'
+ as='int((nf+2)/2) * W/nf * 0.29' pd='2*int((nf+1)/2) * (W/nf + 0.29)' ps='2*int((nf+2)/2) * (W/nf + 0.29)'
+ nrd='0.29 / W' nrs='0.29 / W' sa=0 sb=0 sd=0 mult=1 m=1
XM1[2] net2 Vin VSS net3[2] sky130_fd_pr__nfet_01v8_lvt L=0.5 W=7 nf=1 ad='int((nf+1)/2) * W/nf * 0.29'
+ as='int((nf+2)/2) * W/nf * 0.29' pd='2*int((nf+1)/2) * (W/nf + 0.29)' ps='2*int((nf+2)/2) * (W/nf + 0.29)'
+ nrd='0.29 / W' nrs='0.29 / W' sa=0 sb=0 sd=0 mult=1 m=1
XM1[1] net2 Vin VSS net3[1] sky130_fd_pr__nfet_01v8_lvt L=0.5 W=7 nf=1 ad='int((nf+1)/2) * W/nf * 0.29'
+ as='int((nf+2)/2) * W/nf * 0.29' pd='2*int((nf+1)/2) * (W/nf + 0.29)' ps='2*int((nf+2)/2) * (W/nf + 0.29)'
+ nrd='0.29 / W' nrs='0.29 / W' sa=0 sb=0 sd=0 mult=1 m=1
XM1[0] net2 Vin VSS net3[0] sky130_fd_pr__nfet_01v8_lvt L=0.5 W=7 nf=1 ad='int((nf+1)/2) * W/nf * 0.29'
+ as='int((nf+2)/2) * W/nf * 0.29' pd='2*int((nf+1)/2) * (W/nf + 0.29)' ps='2*int((nf+2)/2) * (W/nf + 0.29)'
+ nrd='0.29 / W' nrs='0.29 / W' sa=0 sb=0 sd=0 mult=1 m=1
XM2[7] net1 Vin VDD net4[7] sky130_fd_pr__pfet_01v8_lvt L=0.5 W=8 nf=1 ad='int((nf+1)/2) * W/nf * 0.29'
+ as='int((nf+2)/2) * W/nf * 0.29' pd='2*int((nf+1)/2) * (W/nf + 0.29)' ps='2*int((nf+2)/2) * (W/nf + 0.29)'
+ nrd='0.29 / W' nrs='0.29 / W' sa=0 sb=0 sd=0 mult=1 m=1
XM2[6] net1 Vin VDD net4[6] sky130_fd_pr__pfet_01v8_lvt L=0.5 W=8 nf=1 ad='int((nf+1)/2) * W/nf * 0.29'
+ as='int((nf+2)/2) * W/nf * 0.29' pd='2*int((nf+1)/2) * (W/nf + 0.29)' ps='2*int((nf+2)/2) * (W/nf + 0.29)'
+ nrd='0.29 / W' nrs='0.29 / W' sa=0 sb=0 sd=0 mult=1 m=1
XM2[5] net1 Vin VDD net4[5] sky130_fd_pr__pfet_01v8_lvt L=0.5 W=8 nf=1 ad='int((nf+1)/2) * W/nf * 0.29'
+ as='int((nf+2)/2) * W/nf * 0.29' pd='2*int((nf+1)/2) * (W/nf + 0.29)' ps='2*int((nf+2)/2) * (W/nf + 0.29)'
+ nrd='0.29 / W' nrs='0.29 / W' sa=0 sb=0 sd=0 mult=1 m=1
XM2[4] net1 Vin VDD net4[4] sky130_fd_pr__pfet_01v8_lvt L=0.5 W=8 nf=1 ad='int((nf+1)/2) * W/nf * 0.29'
+ as='int((nf+2)/2) * W/nf * 0.29' pd='2*int((nf+1)/2) * (W/nf + 0.29)' ps='2*int((nf+2)/2) * (W/nf + 0.29)'
+ nrd='0.29 / W' nrs='0.29 / W' sa=0 sb=0 sd=0 mult=1 m=1
XM2[3] net1 Vin VDD net4[3] sky130_fd_pr__pfet_01v8_lvt L=0.5 W=8 nf=1 ad='int((nf+1)/2) * W/nf * 0.29'
+ as='int((nf+2)/2) * W/nf * 0.29' pd='2*int((nf+1)/2) * (W/nf + 0.29)' ps='2*int((nf+2)/2) * (W/nf + 0.29)'
+ nrd='0.29 / W' nrs='0.29 / W' sa=0 sb=0 sd=0 mult=1 m=1
XM2[2] net1 Vin VDD net4[2] sky130_fd_pr__pfet_01v8_lvt L=0.5 W=8 nf=1 ad='int((nf+1)/2) * W/nf * 0.29'
+ as='int((nf+2)/2) * W/nf * 0.29' pd='2*int((nf+1)/2) * (W/nf + 0.29)' ps='2*int((nf+2)/2) * (W/nf + 0.29)'
+ nrd='0.29 / W' nrs='0.29 / W' sa=0 sb=0 sd=0 mult=1 m=1
XM2[1] net1 Vin VDD net4[1] sky130_fd_pr__pfet_01v8_lvt L=0.5 W=8 nf=1 ad='int((nf+1)/2) * W/nf * 0.29'
+ as='int((nf+2)/2) * W/nf * 0.29' pd='2*int((nf+1)/2) * (W/nf + 0.29)' ps='2*int((nf+2)/2) * (W/nf + 0.29)'
+ nrd='0.29 / W' nrs='0.29 / W' sa=0 sb=0 sd=0 mult=1 m=1
XM2[0] net1 Vin VDD net4[0] sky130_fd_pr__pfet_01v8_lvt L=0.5 W=8 nf=1 ad='int((nf+1)/2) * W/nf * 0.29'
+ as='int((nf+2)/2) * W/nf * 0.29' pd='2*int((nf+1)/2) * (W/nf + 0.29)' ps='2*int((nf+2)/2) * (W/nf + 0.29)'
+ nrd='0.29 / W' nrs='0.29 / W' sa=0 sb=0 sd=0 mult=1 m=1
V1 net1 Vout 0
.save i(v1)
V2 Vout net2 0
.save i(v2)
**.ends
.end
